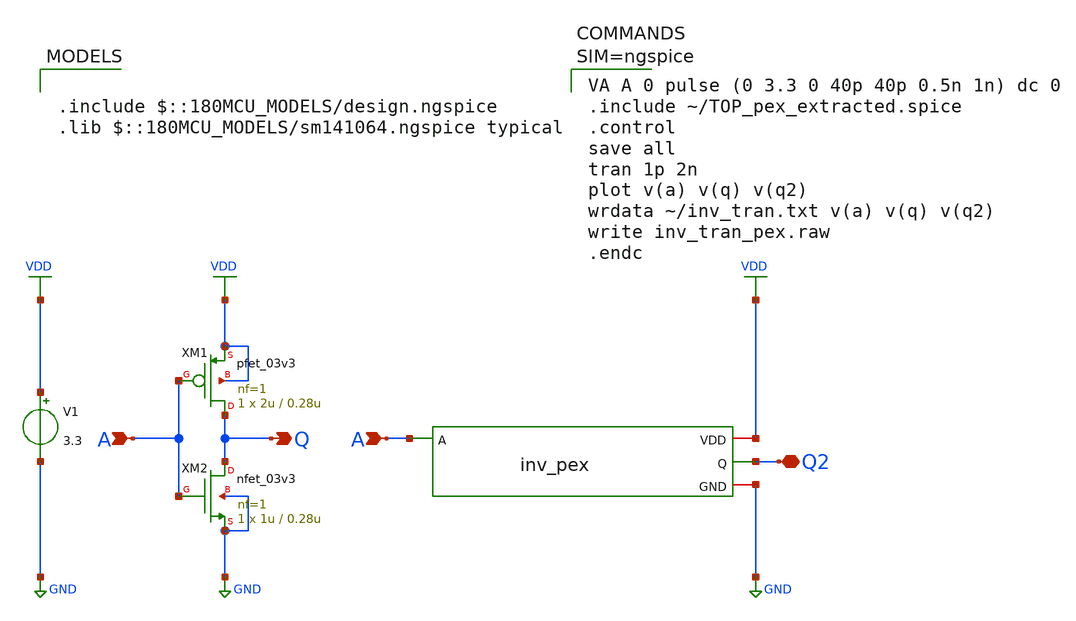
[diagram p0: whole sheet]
** sch_path: inv_tran_pex.sch
**.subckt inv_tran_pex Q Q2 A A
*.opin Q
*.iopin Q2
*.ipin A
*.ipin A
XM1 Q A VDD VDD pfet_03v3 L=0.28u W=2u nf=1 ad='int((nf+1)/2) * W/nf * 0.18u' as='int((nf+2)/2) * W/nf * 0.18u'
+ pd='2*int((nf+1)/2) * (W/nf + 0.18u)' ps='2*int((nf+2)/2) * (W/nf + 0.18u)' nrd='0.18u / W' nrs='0.18u / W'
+ sa=0 sb=0 sd=0 m=1
XM2 Q A GND GND nfet_03v3 L=0.28u W=1u nf=1 ad='int((nf+1)/2) * W/nf * 0.18u' as='int((nf+2)/2) * W/nf * 0.18u'
+ pd='2*int((nf+1)/2) * (W/nf + 0.18u)' ps='2*int((nf+2)/2) * (W/nf + 0.18u)' nrd='0.18u / W' nrs='0.18u / W'
+ sa=0 sb=0 sd=0 m=1
V1 VDD GND 3.3
x1 A Q2 VDD GND TOP
**** begin user architecture code

.include $::180MCU_MODELS/design.ngspice
.lib $::180MCU_MODELS/sm141064.ngspice typical



VA A 0 pulse (0 3.3 0 40p 40p 0.5n 1n) dc 0
.include ~/TOP_pex_extracted.spice
.control
save all
tran 1p 2n
plot v(a) v(q) v(q2)
wrdata ~/inv_tran.txt v(a) v(q) v(q2)
write inv_tran_pex.raw
.endc



**** end user architecture code
**.ends
.GLOBAL VDD
.GLOBAL GND
.end
